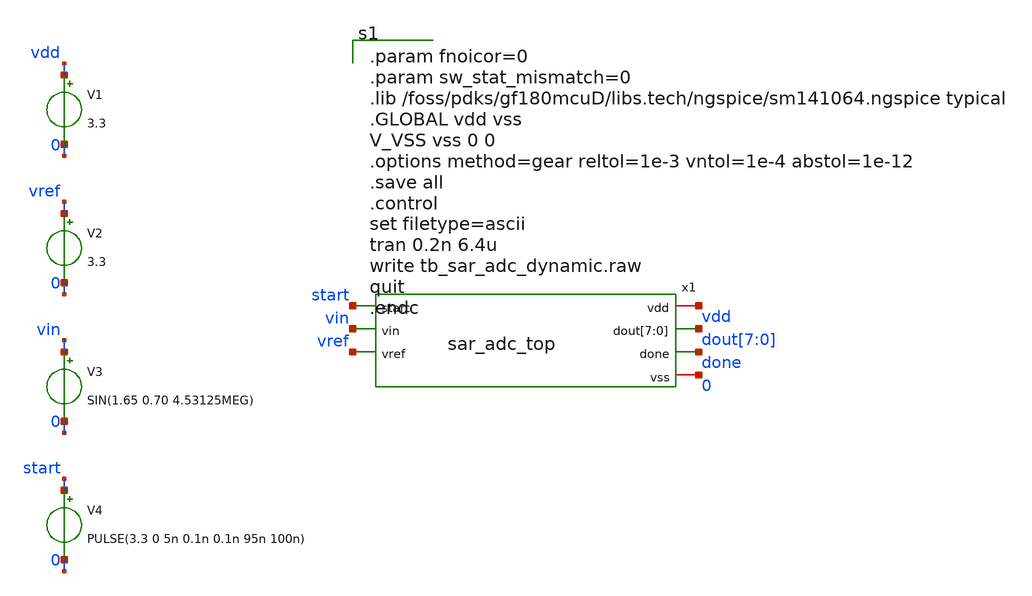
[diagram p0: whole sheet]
** sch_path: xschem/sar_adc/tb_sar_adc_dynamic.sch
**.subckt tb_sar_adc_dynamic
V1 vdd 0 3.3
V2 vref 0 3.3
V3 vin 0 SIN(1.65 0.70 4.53125MEG)
V4 start 0 PULSE(3.3 0 5n 0.1n 0.1n 95n 100n)
x1 vdd start vin dout[7] dout[6] dout[5] dout[4] dout[3] dout[2] dout[1] dout[0] done vref 0
+ sar_adc_top
**.ends
**** begin user architecture code

.param fnoicor=0
.param sw_stat_mismatch=0
.lib /foss/pdks/gf180mcuD/libs.tech/ngspice/sm141064.ngspice typical
.GLOBAL vdd vss
V_VSS vss 0 0
.options method=gear reltol=1e-3 vntol=1e-4 abstol=1e-12
.save all
.control
set filetype=ascii
tran 0.2n 6.4u
write tb_sar_adc_dynamic.raw
quit
.endc

**** end user architecture code
.end
